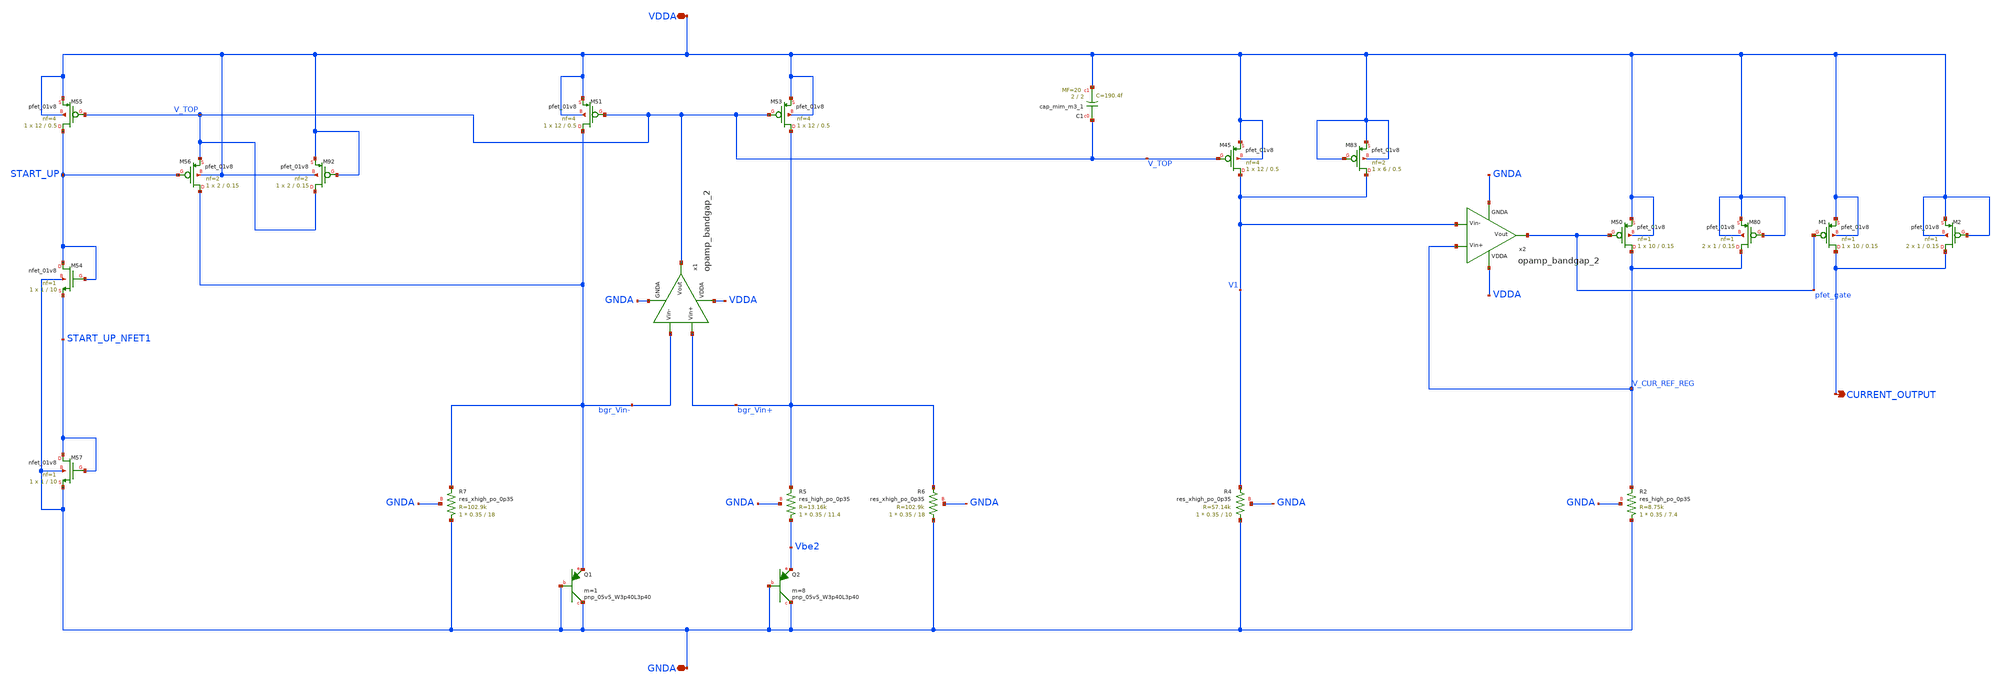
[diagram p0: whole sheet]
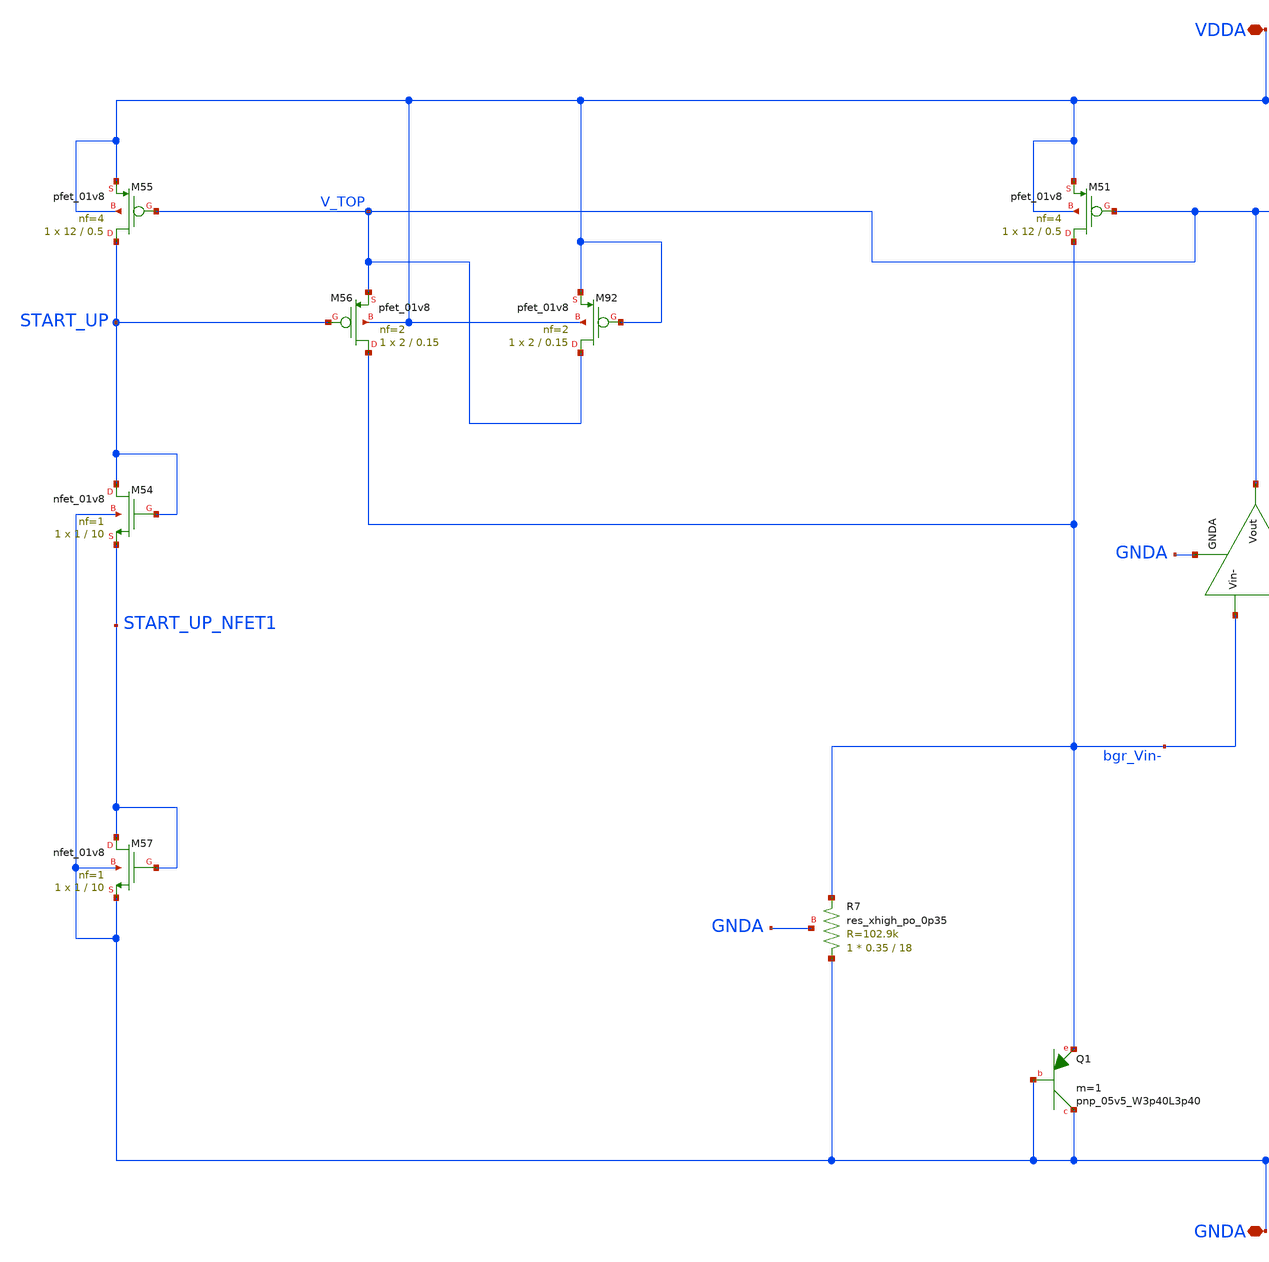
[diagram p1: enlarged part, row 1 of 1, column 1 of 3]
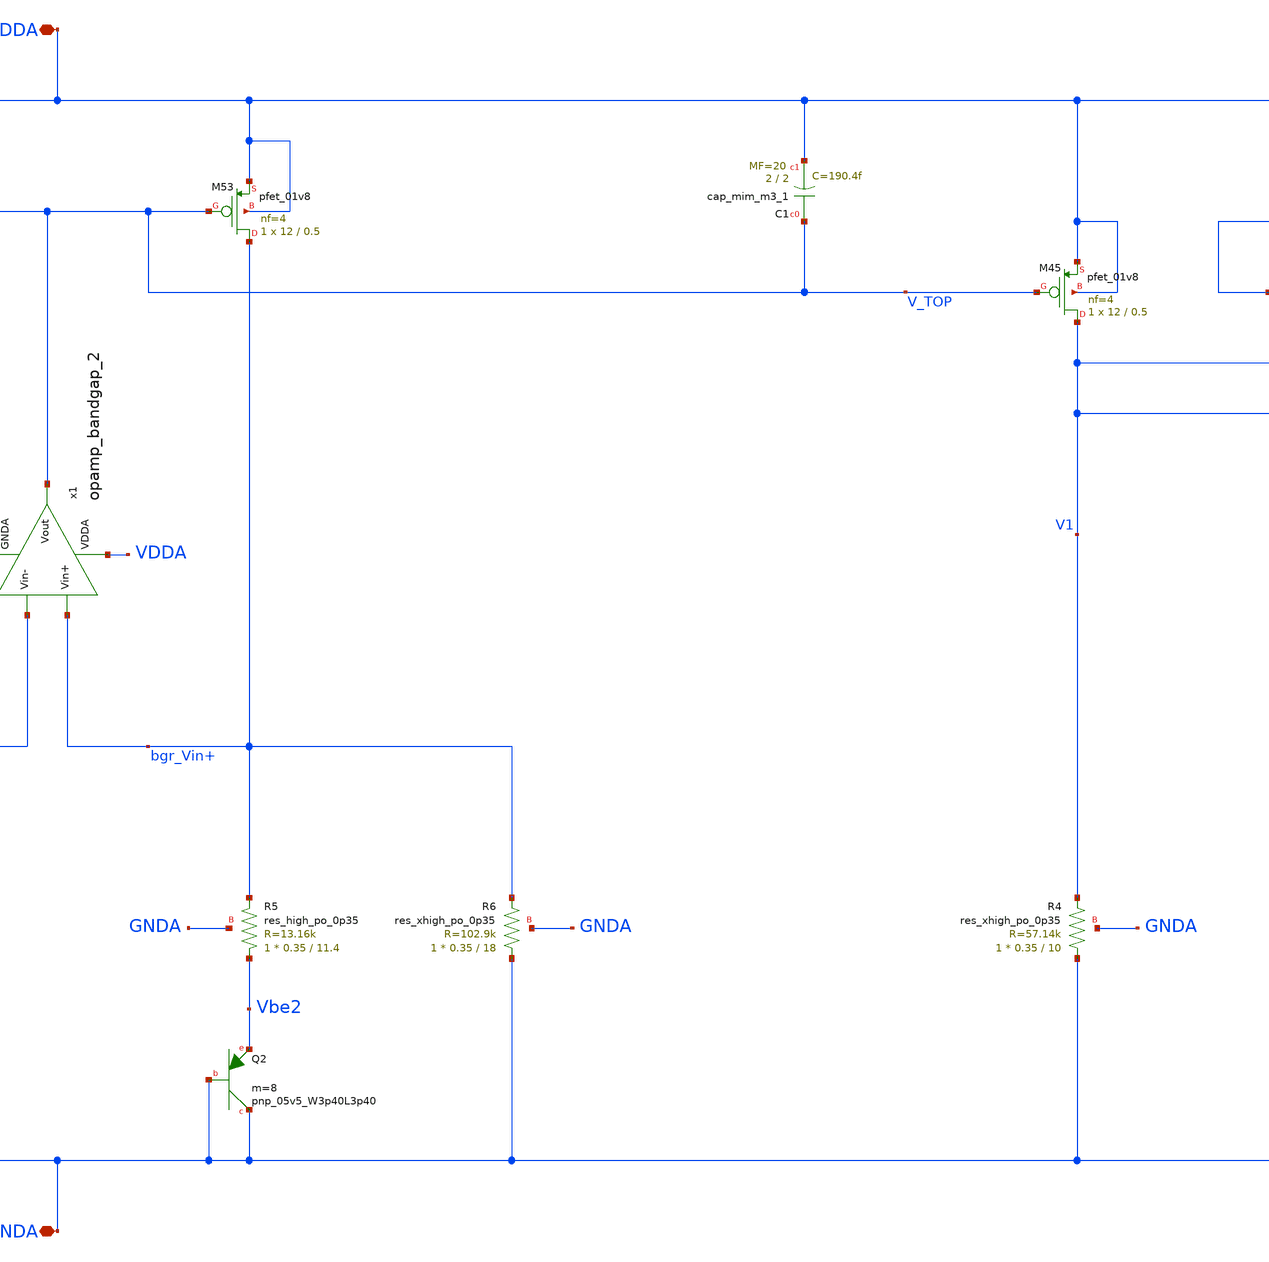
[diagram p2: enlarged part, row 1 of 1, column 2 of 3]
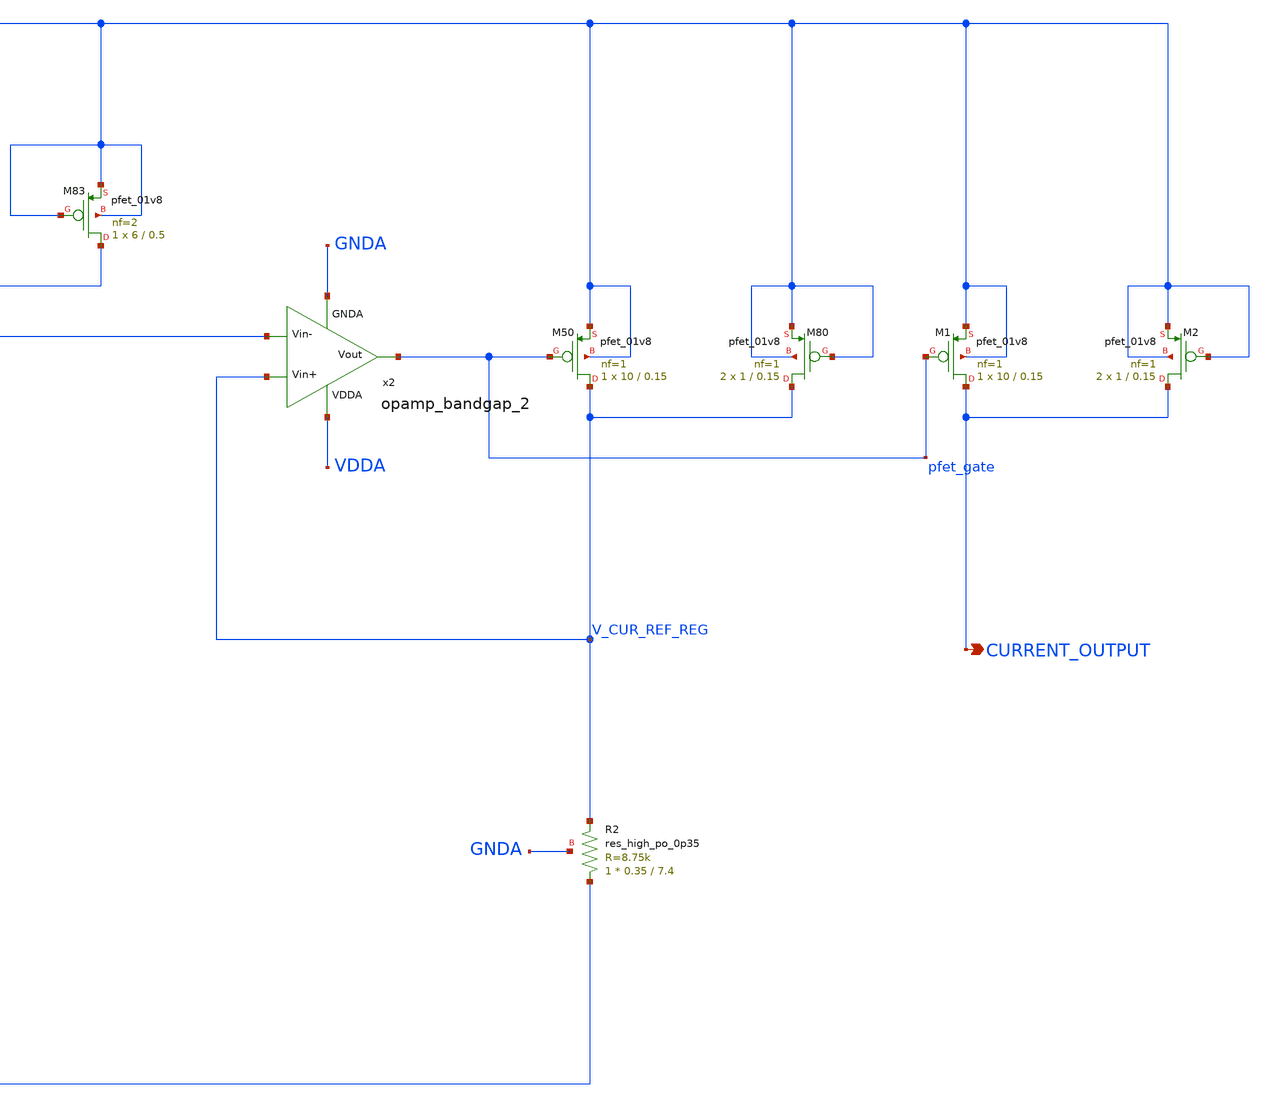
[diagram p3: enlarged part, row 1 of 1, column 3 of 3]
** sch_path: projects/pll/full_pll/xschem_ngspice/bgr_dummy.sch
**.subckt bgr_dummy VDDA GNDA CURRENT_OUTPUT
*.iopin VDDA
*.iopin GNDA
*.opin CURRENT_OUTPUT
XM45 V1 V_TOP VDDA VDDA sky130_fd_pr__pfet_01v8 L=0.5 W=12 nf=4 ad='int((nf+1)/2) * W/nf * 0.29' as='int((nf+2)/2) * W/nf * 0.29'
+ pd='2*int((nf+1)/2) * (W/nf + 0.29)' ps='2*int((nf+2)/2) * (W/nf + 0.29)' nrd='0.29 / W' nrs='0.29 / W'
+ sa=0 sb=0 sd=0 mult=1 m=1
XR4 GNDA V1 GNDA sky130_fd_pr__res_xhigh_po_0p35 L=10 mult=1 m=1
XM50 V_CUR_REF_REG pfet_gate VDDA VDDA sky130_fd_pr__pfet_01v8 L=0.15 W=10 nf=1 ad='int((nf+1)/2) * W/nf * 0.29'
+ as='int((nf+2)/2) * W/nf * 0.29' pd='2*int((nf+1)/2) * (W/nf + 0.29)' ps='2*int((nf+2)/2) * (W/nf + 0.29)'
+ nrd='0.29 / W' nrs='0.29 / W' sa=0 sb=0 sd=0 mult=1 m=1
XC1 V_TOP VDDA sky130_fd_pr__cap_mim_m3_1 W=2 L=2 MF=20 m=20
XQ1 GNDA GNDA bgr_Vin- sky130_fd_pr__pnp_05v5_W3p40L3p40 m=1
XQ2 GNDA GNDA Vbe2 sky130_fd_pr__pnp_05v5_W3p40L3p40 m=8
XM51 bgr_Vin- V_TOP VDDA VDDA sky130_fd_pr__pfet_01v8 L=0.5 W=12 nf=4 ad='int((nf+1)/2) * W/nf * 0.29'
+ as='int((nf+2)/2) * W/nf * 0.29' pd='2*int((nf+1)/2) * (W/nf + 0.29)' ps='2*int((nf+2)/2) * (W/nf + 0.29)'
+ nrd='0.29 / W' nrs='0.29 / W' sa=0 sb=0 sd=0 mult=1 m=1
XM53 bgr_Vin+ V_TOP VDDA VDDA sky130_fd_pr__pfet_01v8 L=0.5 W=12 nf=4 ad='int((nf+1)/2) * W/nf * 0.29'
+ as='int((nf+2)/2) * W/nf * 0.29' pd='2*int((nf+1)/2) * (W/nf + 0.29)' ps='2*int((nf+2)/2) * (W/nf + 0.29)'
+ nrd='0.29 / W' nrs='0.29 / W' sa=0 sb=0 sd=0 mult=1 m=1
XR6 GNDA bgr_Vin+ GNDA sky130_fd_pr__res_xhigh_po_0p35 L=18 mult=1 m=1
XR7 GNDA bgr_Vin- GNDA sky130_fd_pr__res_xhigh_po_0p35 L=18 mult=1 m=1
XM54 START_UP START_UP START_UP_NFET1 GNDA sky130_fd_pr__nfet_01v8 L=10 W=1 nf=1 ad='int((nf+1)/2) * W/nf * 0.29'
+ as='int((nf+2)/2) * W/nf * 0.29' pd='2*int((nf+1)/2) * (W/nf + 0.29)' ps='2*int((nf+2)/2) * (W/nf + 0.29)'
+ nrd='0.29 / W' nrs='0.29 / W' sa=0 sb=0 sd=0 mult=1 m=1
XM55 START_UP V_TOP VDDA VDDA sky130_fd_pr__pfet_01v8 L=0.5 W=12 nf=4 ad='int((nf+1)/2) * W/nf * 0.29'
+ as='int((nf+2)/2) * W/nf * 0.29' pd='2*int((nf+1)/2) * (W/nf + 0.29)' ps='2*int((nf+2)/2) * (W/nf + 0.29)'
+ nrd='0.29 / W' nrs='0.29 / W' sa=0 sb=0 sd=0 mult=1 m=1
XM56 bgr_Vin- START_UP V_TOP VDDA sky130_fd_pr__pfet_01v8 L=0.15 W=2 nf=2 ad='int((nf+1)/2) * W/nf * 0.29'
+ as='int((nf+2)/2) * W/nf * 0.29' pd='2*int((nf+1)/2) * (W/nf + 0.29)' ps='2*int((nf+2)/2) * (W/nf + 0.29)'
+ nrd='0.29 / W' nrs='0.29 / W' sa=0 sb=0 sd=0 mult=1 m=1
XM57 START_UP_NFET1 START_UP_NFET1 GNDA GNDA sky130_fd_pr__nfet_01v8 L=10 W=1 nf=1 ad='int((nf+1)/2) * W/nf * 0.29'
+ as='int((nf+2)/2) * W/nf * 0.29' pd='2*int((nf+1)/2) * (W/nf + 0.29)' ps='2*int((nf+2)/2) * (W/nf + 0.29)'
+ nrd='0.29 / W' nrs='0.29 / W' sa=0 sb=0 sd=0 mult=1 m=1
x1 VDDA V_TOP bgr_Vin- bgr_Vin+ GNDA opamp_bandgap_2
x2 VDDA pfet_gate V1 V_CUR_REF_REG GNDA opamp_bandgap_2
XM80 V_CUR_REF_REG VDDA VDDA VDDA sky130_fd_pr__pfet_01v8 L=0.15 W=1 nf=1 ad='int((nf+1)/2) * W/nf * 0.29'
+ as='int((nf+2)/2) * W/nf * 0.29' pd='2*int((nf+1)/2) * (W/nf + 0.29)' ps='2*int((nf+2)/2) * (W/nf + 0.29)'
+ nrd='0.29 / W' nrs='0.29 / W' sa=0 sb=0 sd=0 mult=2 m=2
XM83 V1 VDDA VDDA VDDA sky130_fd_pr__pfet_01v8 L=0.5 W=6 nf=2 ad='int((nf+1)/2) * W/nf * 0.29' as='int((nf+2)/2) * W/nf * 0.29'
+ pd='2*int((nf+1)/2) * (W/nf + 0.29)' ps='2*int((nf+2)/2) * (W/nf + 0.29)' nrd='0.29 / W' nrs='0.29 / W'
+ sa=0 sb=0 sd=0 mult=1 m=1
XM92 V_TOP VDDA VDDA VDDA sky130_fd_pr__pfet_01v8 L=0.15 W=2 nf=2 ad='int((nf+1)/2) * W/nf * 0.29' as='int((nf+2)/2) * W/nf * 0.29'
+ pd='2*int((nf+1)/2) * (W/nf + 0.29)' ps='2*int((nf+2)/2) * (W/nf + 0.29)' nrd='0.29 / W' nrs='0.29 / W'
+ sa=0 sb=0 sd=0 mult=1 m=1
XM1 CURRENT_OUTPUT pfet_gate VDDA VDDA sky130_fd_pr__pfet_01v8 L=0.15 W=10 nf=1 ad='int((nf+1)/2) * W/nf * 0.29'
+ as='int((nf+2)/2) * W/nf * 0.29' pd='2*int((nf+1)/2) * (W/nf + 0.29)' ps='2*int((nf+2)/2) * (W/nf + 0.29)'
+ nrd='0.29 / W' nrs='0.29 / W' sa=0 sb=0 sd=0 mult=1 m=1
XM2 CURRENT_OUTPUT VDDA VDDA VDDA sky130_fd_pr__pfet_01v8 L=0.15 W=1 nf=1 ad='int((nf+1)/2) * W/nf * 0.29'
+ as='int((nf+2)/2) * W/nf * 0.29' pd='2*int((nf+1)/2) * (W/nf + 0.29)' ps='2*int((nf+2)/2) * (W/nf + 0.29)'
+ nrd='0.29 / W' nrs='0.29 / W' sa=0 sb=0 sd=0 mult=2 m=2
XR2 GNDA V_CUR_REF_REG GNDA sky130_fd_pr__res_high_po_0p35 L=7.4 mult=1 m=1
XR5 Vbe2 bgr_Vin+ GNDA sky130_fd_pr__res_high_po_0p35 L=11.4 mult=1 m=1
**.ends

* expanding   symbol:
*+  /foss/designs/my_design/projects/bandgapref/xschem_ngspice/new_files/opamp_bandgap_2.sym # of pins=5
** sym_path: projects/bandgapref/xschem_ngspice/new_files/opamp_bandgap_2.sym
** sch_path: projects/bandgapref/xschem_ngspice/new_files/opamp_bandgap_2.sch
.subckt opamp_bandgap_2 VDDA Vout Vin- Vin+ GNDA
*.ipin Vin+
*.opin Vout
*.ipin Vin-
*.ipin GNDA
*.ipin VDDA
XM1 V_p VDDA GNDA GNDA sky130_fd_pr__nfet_01v8 L=5 W=2.5 nf=1 ad='int((nf+1)/2) * W/nf * 0.29' as='int((nf+2)/2) * W/nf * 0.29'
+ pd='2*int((nf+1)/2) * (W/nf + 0.29)' ps='2*int((nf+2)/2) * (W/nf + 0.29)' nrd='0.29 / W' nrs='0.29 / W'
+ sa=0 sb=0 sd=0 mult=1 m=1
XM2 V_mirror Vin- V_p GNDA sky130_fd_pr__nfet_01v8 L=0.2 W=2.5 nf=1 ad='int((nf+1)/2) * W/nf * 0.29'
+ as='int((nf+2)/2) * W/nf * 0.29' pd='2*int((nf+1)/2) * (W/nf + 0.29)' ps='2*int((nf+2)/2) * (W/nf + 0.29)'
+ nrd='0.29 / W' nrs='0.29 / W' sa=0 sb=0 sd=0 mult=1 m=1
XM3 1st_Vout Vin+ V_p GNDA sky130_fd_pr__nfet_01v8 L=0.2 W=2.5 nf=1 ad='int((nf+1)/2) * W/nf * 0.29'
+ as='int((nf+2)/2) * W/nf * 0.29' pd='2*int((nf+1)/2) * (W/nf + 0.29)' ps='2*int((nf+2)/2) * (W/nf + 0.29)'
+ nrd='0.29 / W' nrs='0.29 / W' sa=0 sb=0 sd=0 mult=1 m=1
XM5 V_mirror V_mirror VDDA VDDA sky130_fd_pr__pfet_01v8 L=0.2 W=6 nf=2 ad='int((nf+1)/2) * W/nf * 0.29'
+ as='int((nf+2)/2) * W/nf * 0.29' pd='2*int((nf+1)/2) * (W/nf + 0.29)' ps='2*int((nf+2)/2) * (W/nf + 0.29)'
+ nrd='0.29 / W' nrs='0.29 / W' sa=0 sb=0 sd=0 mult=1 m=1
XM6 1st_Vout V_mirror VDDA VDDA sky130_fd_pr__pfet_01v8 L=0.2 W=6 nf=2 ad='int((nf+1)/2) * W/nf * 0.29'
+ as='int((nf+2)/2) * W/nf * 0.29' pd='2*int((nf+1)/2) * (W/nf + 0.29)' ps='2*int((nf+2)/2) * (W/nf + 0.29)'
+ nrd='0.29 / W' nrs='0.29 / W' sa=0 sb=0 sd=0 mult=1 m=1
XM4 Vout VDDA GNDA GNDA sky130_fd_pr__nfet_01v8 L=5 W=2.5 nf=1 ad='int((nf+1)/2) * W/nf * 0.29' as='int((nf+2)/2) * W/nf * 0.29'
+ pd='2*int((nf+1)/2) * (W/nf + 0.29)' ps='2*int((nf+2)/2) * (W/nf + 0.29)' nrd='0.29 / W' nrs='0.29 / W'
+ sa=0 sb=0 sd=0 mult=1 m=1
XM7 Vout 1st_Vout VDDA VDDA sky130_fd_pr__pfet_01v8 L=0.2 W=6 nf=2 ad='int((nf+1)/2) * W/nf * 0.29' as='int((nf+2)/2) * W/nf * 0.29'
+ pd='2*int((nf+1)/2) * (W/nf + 0.29)' ps='2*int((nf+2)/2) * (W/nf + 0.29)' nrd='0.29 / W' nrs='0.29 / W'
+ sa=0 sb=0 sd=0 mult=1 m=1
XC1 1st_Vout cap_res sky130_fd_pr__cap_mim_m3_1 W=2 L=2 MF=20 m=20
XM8 Vout VDDA VDDA VDDA sky130_fd_pr__pfet_01v8 L=0.2 W=1 nf=1 ad='int((nf+1)/2) * W/nf * 0.29' as='int((nf+2)/2) * W/nf * 0.29'
+ pd='2*int((nf+1)/2) * (W/nf + 0.29)' ps='2*int((nf+2)/2) * (W/nf + 0.29)' nrd='0.29 / W' nrs='0.29 / W'
+ sa=0 sb=0 sd=0 mult=2 m=2
XR1 Vout cap_res GNDA sky130_fd_pr__res_high_po_0p69 L=5 mult=1 m=1
.ends

.end
